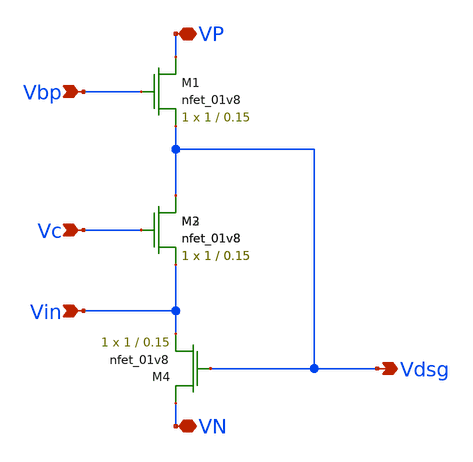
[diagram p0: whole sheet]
** sch_path: fvf.sch
**.subckt fvf VP VN Vbp Vc Vin Vdsg
*.iopin VP
*.iopin VN
*.ipin Vbp
*.ipin Vc
*.ipin Vin
*.opin Vdsg
XM1 VP Vbp Vdsg GND sky130_fd_pr__nfet_01v8 L=0.15 W=1 nf=1 ad='int((nf+1)/2) * W/nf * 0.29' as='int((nf+2)/2) * W/nf * 0.29'
+ pd='2*int((nf+1)/2) * (W/nf + 0.29)' ps='2*int((nf+2)/2) * (W/nf + 0.29)' nrd='0.29 / W' nrs='0.29 / W'
+ sa=0 sb=0 sd=0 mult=1 m=1
XM2 Vdsg Vc Vin GND sky130_fd_pr__nfet_01v8 L=0.15 W=1 nf=1 ad='int((nf+1)/2) * W/nf * 0.29' as='int((nf+2)/2) * W/nf * 0.29'
+ pd='2*int((nf+1)/2) * (W/nf + 0.29)' ps='2*int((nf+2)/2) * (W/nf + 0.29)' nrd='0.29 / W' nrs='0.29 / W'
+ sa=0 sb=0 sd=0 mult=1 m=1
XM3 Vdsg Vc Vin GND sky130_fd_pr__nfet_01v8 L=0.15 W=1 nf=1 ad='int((nf+1)/2) * W/nf * 0.29' as='int((nf+2)/2) * W/nf * 0.29'
+ pd='2*int((nf+1)/2) * (W/nf + 0.29)' ps='2*int((nf+2)/2) * (W/nf + 0.29)' nrd='0.29 / W' nrs='0.29 / W'
+ sa=0 sb=0 sd=0 mult=1 m=1
XM4 VN Vdsg Vin GND sky130_fd_pr__nfet_01v8 L=0.15 W=1 nf=1 ad='int((nf+1)/2) * W/nf * 0.29' as='int((nf+2)/2) * W/nf * 0.29'
+ pd='2*int((nf+1)/2) * (W/nf + 0.29)' ps='2*int((nf+2)/2) * (W/nf + 0.29)' nrd='0.29 / W' nrs='0.29 / W'
+ sa=0 sb=0 sd=0 mult=1 m=1
**.ends
.end
